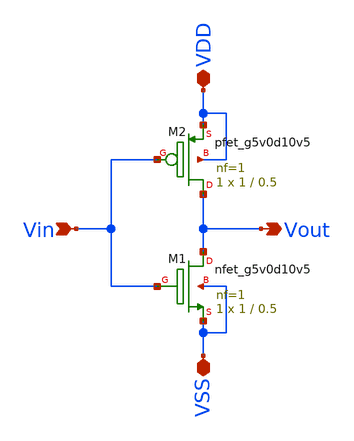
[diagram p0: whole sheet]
** sch_path: analog/schematics/inverter.sch
**.subckt inverter Vout VDD VSS Vin
*.opin Vout
*.iopin VDD
*.iopin VSS
*.ipin Vin
XM2 Vout Vin VDD VDD sky130_fd_pr__pfet_g5v0d10v5 L=0.5 W=1 nf=1 ad='int((nf+1)/2) * W/nf * 0.29' as='int((nf+2)/2) * W/nf * 0.29'
+ pd='2*int((nf+1)/2) * (W/nf + 0.29)' ps='2*int((nf+2)/2) * (W/nf + 0.29)' nrd='0.29 / W' nrs='0.29 / W'
+ sa=0 sb=0 sd=0 mult=1 m=1
XM1 Vout Vin VSS VSS sky130_fd_pr__nfet_g5v0d10v5 L=0.5 W=1 nf=1 ad='int((nf+1)/2) * W/nf * 0.29' as='int((nf+2)/2) * W/nf * 0.29'
+ pd='2*int((nf+1)/2) * (W/nf + 0.29)' ps='2*int((nf+2)/2) * (W/nf + 0.29)' nrd='0.29 / W' nrs='0.29 / W'
+ sa=0 sb=0 sd=0 mult=1 m=1
**.ends
.end
